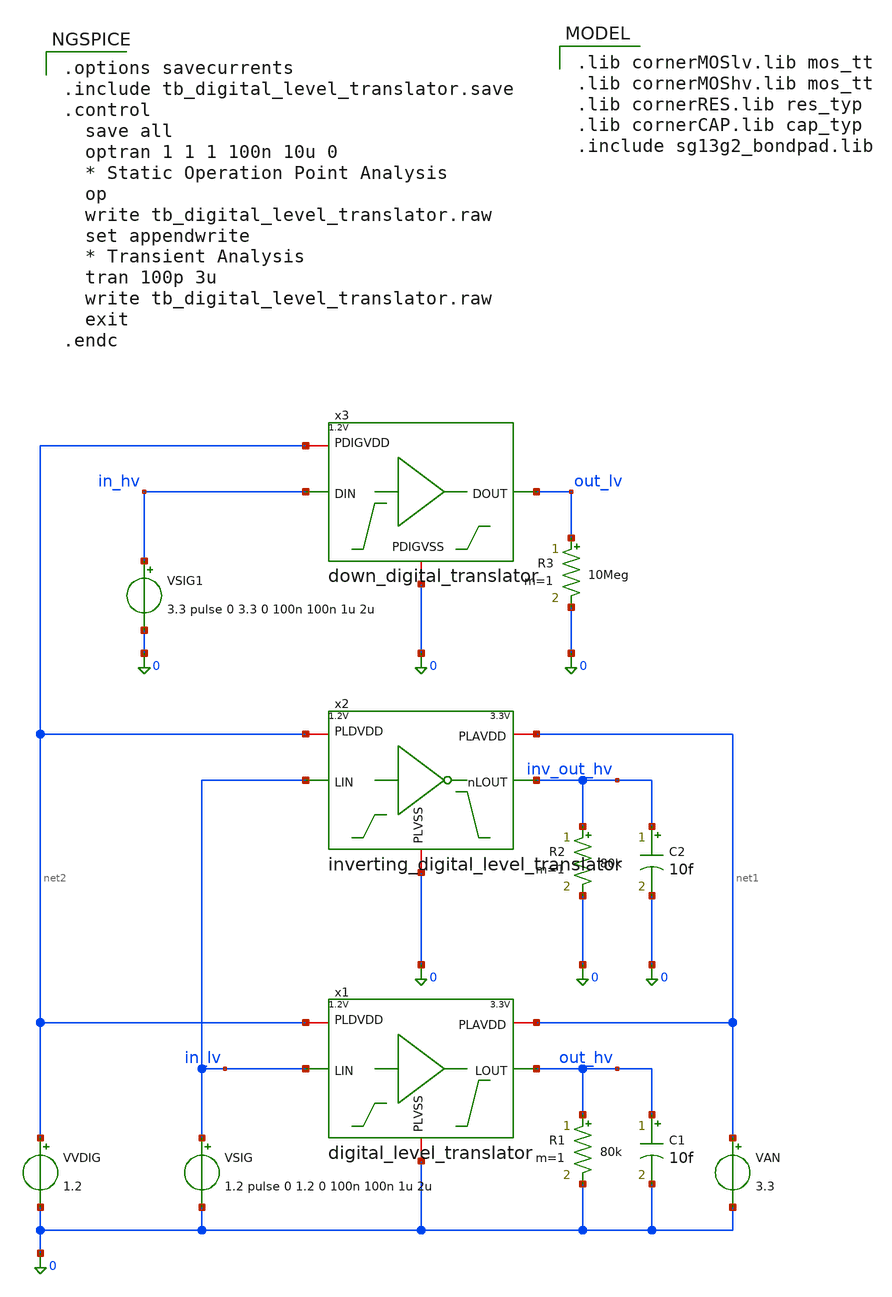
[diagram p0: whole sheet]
** sch_path: xschem/tb_digital_level_translator.sch
**.subckt tb_digital_level_translator
x1 net1 net2 in_lv out_hv 0 digital_level_translator
VVDIG net2 0 1.2
VAN net1 0 3.3
VSIG in_lv 0 1.2 pulse 0 1.2 0 100n 100n 1u 2u
R1 out_hv 0 80k m=1
C1 out_hv 0 10f m=1
x2 net1 net2 in_lv inv_out_hv 0 inverting_digital_level_translator
R2 inv_out_hv 0 80k m=1
C2 inv_out_hv 0 10f m=1
x3 net2 in_hv out_lv 0 down_digital_translator
R3 out_lv 0 10Meg m=1
VSIG1 in_hv 0 3.3 pulse 0 3.3 0 100n 100n 1u 2u
**** begin user architecture code

.options savecurrents
.include tb_digital_level_translator.save
.control
  save all
  optran 1 1 1 100n 10u 0
  * Static Operation Point Analysis
  op
  write tb_digital_level_translator.raw
  set appendwrite
  * Transient Analysis
  tran 100p 3u
  write tb_digital_level_translator.raw
  exit
.endc



.lib cornerMOSlv.lib mos_tt
.lib cornerMOShv.lib mos_tt
.lib cornerRES.lib res_typ
.lib cornerCAP.lib cap_typ
.include sg13g2_bondpad.lib


**** end user architecture code
**.ends

* expanding   symbol:  digital_level_translator.sym # of pins=5
** sym_path: xschem/digital_level_translator.sym
** sch_path: xschem/digital_level_translator.sch
.subckt digital_level_translator PLAVDD PLDVDD LIN LOUT PLVSS
*.iopin PLAVDD
*.iopin PLVSS
*.iopin PLDVDD
*.ipin LIN
*.opin LOUT
XM1 n_lin_buf LIN PLVSS PLVSS sg13_lv_nmos w=0.15u l=0.13u ng=1 m=1 mm_ok=1
XM2 n_lin_buf LIN PLDVDD PLDVDD sg13_lv_pmos w=0.3u l=0.13u ng=1 m=1 mm_ok=1
XM3 lin_buf n_lin_buf PLVSS PLVSS sg13_lv_nmos w=0.15u l=0.13u ng=1 m=1 mm_ok=1
XM4 lin_buf n_lin_buf PLDVDD PLDVDD sg13_lv_pmos w=0.3u l=0.13u ng=1 m=1 mm_ok=1
XM5 q_unbf n_lin_buf PLVSS PLVSS sg13_hv_nmos w=1u l=0.45u ng=1 m=1 mm_ok=1
XM6 n_q_unbf lin_buf PLVSS PLVSS sg13_hv_nmos w=1u l=0.45u ng=1 m=1 mm_ok=1
XM7 n_q_unbf q_unbf PLAVDD PLAVDD sg13_hv_pmos w=0.3u l=0.45u ng=1 m=1 mm_ok=1
XM9 LOUT n_q_unbf PLVSS PLVSS sg13_hv_nmos w=0.3u l=0.45u ng=1 m=4 mm_ok=1
XM10 LOUT n_q_unbf PLAVDD PLAVDD sg13_hv_pmos w=0.6u l=0.45u ng=1 m=4 mm_ok=1
XM8 q_unbf n_q_unbf PLAVDD PLAVDD sg13_hv_pmos w=0.3u l=0.45u ng=1 m=1 mm_ok=1
.ends


* expanding   symbol:  inverting_digital_level_translator.sym # of pins=5
** sym_path: xschem/inverting_digital_level_translator.sym
** sch_path: xschem/inverting_digital_level_translator.sch
.subckt inverting_digital_level_translator PLAVDD PLDVDD LIN nLOUT PLVSS
*.iopin PLAVDD
*.iopin PLVSS
*.iopin PLDVDD
*.ipin LIN
*.opin nLOUT
XM1 n_lin_buf net1 PLVSS PLVSS sg13_lv_nmos w=0.15u l=0.13u ng=1 m=1 mm_ok=1
XM2 n_lin_buf net1 PLDVDD PLDVDD sg13_lv_pmos w=0.3u l=0.13u ng=1 m=1 mm_ok=1
XM3 lin_buf n_lin_buf PLVSS PLVSS sg13_lv_nmos w=0.15u l=0.13u ng=1 m=1 mm_ok=1
XM4 lin_buf n_lin_buf PLDVDD PLDVDD sg13_lv_pmos w=0.3u l=0.13u ng=1 m=1 mm_ok=1
XM5 q_unbf n_lin_buf PLVSS PLVSS sg13_hv_nmos w=1u l=0.45u ng=1 m=1 mm_ok=1
XM6 n_q_unbf lin_buf PLVSS PLVSS sg13_hv_nmos w=1u l=0.45u ng=1 m=1 mm_ok=1
XM7 n_q_unbf q_unbf PLAVDD PLAVDD sg13_hv_pmos w=0.3u l=0.45u ng=1 m=1 mm_ok=1
XM9 nLOUT n_q_unbf PLVSS PLVSS sg13_hv_nmos w=0.3u l=0.45u ng=1 m=4 mm_ok=1
XM10 nLOUT n_q_unbf PLAVDD PLAVDD sg13_hv_pmos w=0.6u l=0.45u ng=1 m=4 mm_ok=1
XM8 q_unbf n_q_unbf PLAVDD PLAVDD sg13_hv_pmos w=0.3u l=0.45u ng=1 m=1 mm_ok=1
XM11 net1 LIN PLVSS PLVSS sg13_lv_nmos w=0.15u l=0.13u ng=1 m=1 mm_ok=1
XM12 net1 LIN PLDVDD PLDVDD sg13_lv_pmos w=0.3u l=0.13u ng=1 m=1 mm_ok=1
.ends


* expanding   symbol:  down_digital_translator.sym # of pins=4
** sym_path: xschem/down_digital_translator.sym
** sch_path: xschem/down_digital_translator.sch
.subckt down_digital_translator PDIGVDD DIN DOUT PDIGVSS
*.iopin PDIGVDD
*.ipin DIN
*.opin DOUT
*.iopin PDIGVSS
XM1 net1 DIN PDIGVSS PDIGVSS sg13_hv_nmos w=0.3u l=0.45u ng=1 m=1 mm_ok=1
XM2 net1 DIN PDIGVDD PDIGVDD sg13_hv_pmos w=0.6u l=0.45u ng=1 m=1 mm_ok=1
XM3 DOUT net1 PDIGVSS PDIGVSS sg13_hv_nmos w=0.3u l=0.45u ng=1 m=1 mm_ok=1
XM4 DOUT net1 PDIGVDD PDIGVDD sg13_hv_pmos w=0.6u l=0.45u ng=1 m=1 mm_ok=1
.ends

.end
